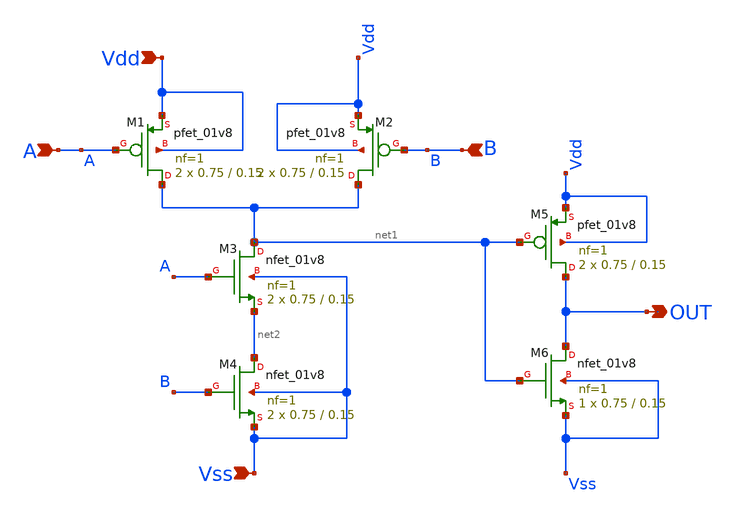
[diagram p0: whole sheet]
** sch_path: icdesign/sch/And/AND.sch
**.subckt AND Vss Vdd A OUT B
*.ipin Vss
*.ipin Vdd
*.ipin A
*.opin OUT
*.ipin B
XM1 net1 A Vdd Vdd sky130_fd_pr__pfet_01v8 L=0.15 W=0.75 nf=1 ad='int((nf+1)/2) * W/nf * 0.29' as='int((nf+2)/2) * W/nf * 0.29'
+ pd='2*int((nf+1)/2) * (W/nf + 0.29)' ps='2*int((nf+2)/2) * (W/nf + 0.29)' nrd='0.29 / W' nrs='0.29 / W'
+ sa=0 sb=0 sd=0 mult=2 m=2
XM2 net1 B Vdd Vdd sky130_fd_pr__pfet_01v8 L=0.15 W=0.75 nf=1 ad='int((nf+1)/2) * W/nf * 0.29' as='int((nf+2)/2) * W/nf * 0.29'
+ pd='2*int((nf+1)/2) * (W/nf + 0.29)' ps='2*int((nf+2)/2) * (W/nf + 0.29)' nrd='0.29 / W' nrs='0.29 / W'
+ sa=0 sb=0 sd=0 mult=2 m=2
XM5 OUT net1 Vdd Vdd sky130_fd_pr__pfet_01v8 L=0.15 W=0.75 nf=1 ad='int((nf+1)/2) * W/nf * 0.29' as='int((nf+2)/2) * W/nf * 0.29'
+ pd='2*int((nf+1)/2) * (W/nf + 0.29)' ps='2*int((nf+2)/2) * (W/nf + 0.29)' nrd='0.29 / W' nrs='0.29 / W'
+ sa=0 sb=0 sd=0 mult=2 m=2
XM6 OUT net1 Vss Vss sky130_fd_pr__nfet_01v8 L=0.15 W=0.75 nf=1 ad='int((nf+1)/2) * W/nf * 0.29' as='int((nf+2)/2) * W/nf * 0.29'
+ pd='2*int((nf+1)/2) * (W/nf + 0.29)' ps='2*int((nf+2)/2) * (W/nf + 0.29)' nrd='0.29 / W' nrs='0.29 / W'
+ sa=0 sb=0 sd=0 mult=1 m=1
XM3 net1 A net2 Vss sky130_fd_pr__nfet_01v8 L=0.15 W=0.75 nf=1 ad='int((nf+1)/2) * W/nf * 0.29' as='int((nf+2)/2) * W/nf * 0.29'
+ pd='2*int((nf+1)/2) * (W/nf + 0.29)' ps='2*int((nf+2)/2) * (W/nf + 0.29)' nrd='0.29 / W' nrs='0.29 / W'
+ sa=0 sb=0 sd=0 mult=2 m=2
XM4 net2 B Vss Vss sky130_fd_pr__nfet_01v8 L=0.15 W=0.75 nf=1 ad='int((nf+1)/2) * W/nf * 0.29' as='int((nf+2)/2) * W/nf * 0.29'
+ pd='2*int((nf+1)/2) * (W/nf + 0.29)' ps='2*int((nf+2)/2) * (W/nf + 0.29)' nrd='0.29 / W' nrs='0.29 / W'
+ sa=0 sb=0 sd=0 mult=2 m=2
**.ends
.end
